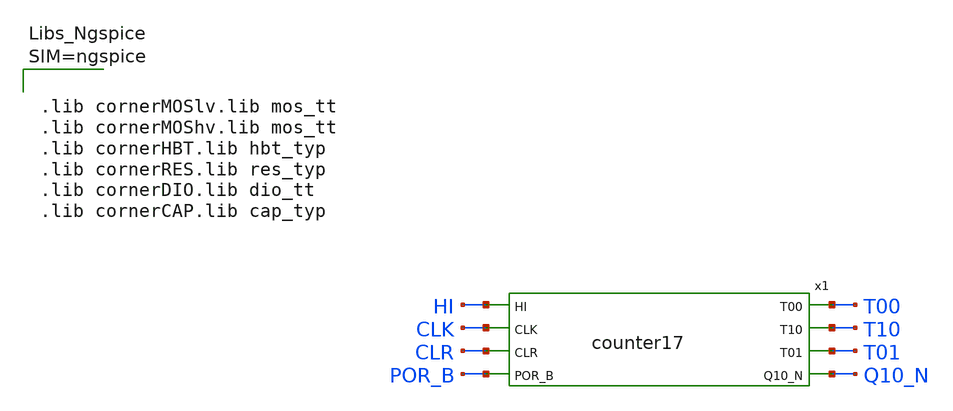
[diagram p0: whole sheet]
** sch_path: design/blocks/counter_bit/schematic/counter17_tb.sch
**.subckt counter17_tb
x1 T00 HI T10 CLK CLR T01 Q10_N POR_B VDD VSS counter17
**** begin user architecture code



.lib cornerMOSlv.lib mos_tt
.lib cornerMOShv.lib mos_tt
.lib cornerHBT.lib hbt_typ
.lib cornerRES.lib res_typ
.lib cornerDIO.lib dio_tt
.lib cornerCAP.lib cap_typ






* ============================================================
* counter17_tb -- validacion a nivel transistor de counter17 (IHP SG13G2)
* 17 x one_bit (D = (Q xor CI)&~CLR, CO = Q&CI), tomas T00 = Q13&Q11,
* T10 = Q16&Q15&Q12, T01 = Q10, Q10_N.
* Corner MOS: editar la linea .lib (mos_tt / mos_ss / ...)
* Barre T = -40/27/85 C  x  VDD = 1.08/1.2/1.32 V dentro de .control
* CLK = 50 MHz (celdas estaticas: la funcion no depende de f; con 1025 ciclos
* a 10 kHz la corrida seria de 100 ms). Flancos de subida en 10n + k*20n;
* entradas cambian en el flanco de bajada (20n + k*20n).
* Secuencia (k = numero de flanco):
*   k = 0        POR_B = 0                 -> cuenta 0 (reset asincronico)
*   k = 1..39    cuenta = k                -> se verifica Q0..Q5 en cada ciclo
*   k = 40, 41   CLR = 1                   -> cuenta 0 (borrado sincronico)
*   k = 42..51   cuenta = k - 41
*   t = 1050n    POR_B = 0 a mitad de ciclo con cuenta 10 -> Q3 y Q1 bajan sin flanco
* Las tomas (T01 = 1024, T00 = 10240, T10 = 102400 ciclos) no se alcanzan a nivel
* transistor en un tiempo razonable (>10 min por caso solo para T01): se verifican
* con el netlist exportado en Icarus (counter17_logic_tb.v). Aca se exige que
* T00, T10 y T01 no tengan glitches y que Q10_N quede en 1.
.global VDD VSS
.param vdd=1.2

* carga en las salidas: una entrada de celda (como en wd_control)
xl0 T00B T00 VDD VSS sg13g2_inv_1
xl1 T10B T10 VDD VSS sg13g2_inv_1
xl2 T01B T01 VDD VSS sg13g2_inv_1
xl3 Q10NB Q10_N VDD VSS sg13g2_inv_1

* ---------- fuentes ----------
V_VDD VDD 0 PWL(0 0 5n {vdd})
V_VSS VSS 0 0
V_HI  HI  0 {vdd}
V_CLK CLK 0 PULSE(0 {vdd} 10n 0.1n 0.1n 10n 20n)
V_POR POR_B 0 PWL(0 0 20n 0 20.01n {vdd} 1050n {vdd} 1050.01n 0)
V_CLR CLR   0 PWL(0 0 800n 0 800.01n {vdd} 840n {vdd} 840.01n 0)

.option method=gear maxord=2 reltol=1e-3
.save v(clk) v(clr) v(por_b) v(t00) v(t10) v(t01) v(q10_n) v(x1.q0) v(x1.q1) v(x1.q2) v(x1.q3) v(x1.q4) v(x1.q5)

.control
set noaskquit
compose tlist values -40 27 85
compose vlist values 1.08 1.2 1.32
let npass = 0
let ncase = 0
let it = 0
while it lt 3
 let iv = 0
 while iv lt 3
  let tt = tlist[it]
  let vv = vlist[iv]
  alterparam vdd = $&vv
  reset
  option temp = $&tt
  tran 0.1n 1100n 0 0.5n
  * reintento si ngspice aborta ('timestep too small' = artefacto numerico)
  let nt = length(time)
  let tend = time[nt-1]
  if tend lt 1090n
   echo REINTENTO T=$&tt VDD=$&vv con tmax=0.25n (aborto en t=$&tend)
   reset
   option temp = $&tt
   tran 0.05n 1100n 0 0.25n
  end
  let vh = vv/2
  * --- 1) cuenta en los bits 0..5 (muestreo a mitad de ciclo, 15 ns despues del flanco) ---
  let nok = 0
  let nchk = 0
  let k = 0
  while k lt 51
   let ts = 25n + k*20n
   if k lt 40
    let nexp = k
   else
    if k lt 42
     let nexp = 0
    else
     let nexp = k - 41
    end
   end
   meas tran b0 FIND v(x1.q0) AT=$&ts
   meas tran b1 FIND v(x1.q1) AT=$&ts
   meas tran b2 FIND v(x1.q2) AT=$&ts
   meas tran b3 FIND v(x1.q3) AT=$&ts
   meas tran b4 FIND v(x1.q4) AT=$&ts
   meas tran b5 FIND v(x1.q5) AT=$&ts
   let n = (b0 gt vh) + 2*(b1 gt vh) + 4*(b2 gt vh) + 8*(b3 gt vh) + 16*(b4 gt vh) + 32*(b5 gt vh)
   if n eq nexp
    let nok = nok + 1
   else
    echo FALLA cuenta: k=$&k leida=$&n esperada=$&nexp
   end
   let nchk = nchk + 1
   let k = k + 1
  end
  * --- 2) tomas sin glitches y Q10_N = 1 (cuenta < 1024) ---
  meas tran m00 MAX v(t00) FROM=30n TO=1040n
  meas tran m10 MAX v(t10) FROM=30n TO=1040n
  meas tran m01 MAX v(t01) FROM=30n TO=1040n
  meas tran mqn MIN v(q10_n) FROM=30n TO=1040n
  let p_tap = (m00 lt 0.3*vv) & (m10 lt 0.3*vv) & (m01 lt 0.3*vv) & (mqn gt 0.7*vv)
  * --- 3) tiempo CLK->Q del bit 0 (flanco 1, 30n) ---
  let tcq = -1
  meas tran tcq WHEN v(x1.q0)=$&vh RISE=1
  let dcq = (tcq - 30n)*1e9
  * --- 4) reset asincronico: POR_B baja en 1050n con cuenta 10 (Q3 = 1) ---
  meas tran q3a FIND v(x1.q3) AT=1045n
  let tra = -1
  meas tran tra WHEN v(x1.q3)=$&vh FALL=LAST
  let da = (tra - 1050n)*1e9
  let p_rst = (q3a gt vh) & (da gt 0) & (da lt 2)
  let pass = (nok eq nchk) & p_tap & p_rst & (dcq gt 0) & (dcq lt 2)
  if pass > 0.5
   echo CASO T=$&tt VDD=$&vv : PASS  cuenta=$&nok/$&nchk tCQ=$&dcq ns reset=$&da ns
   let npass = npass + 1
  else
   echo CASO T=$&tt VDD=$&vv : FAIL  cuenta=$&nok/$&nchk tomas=$&p_tap tCQ=$&dcq reset=$&p_rst
  end
  set wr_singlescale
  wrdata counter17_{$&tt}_{$&vv}.txt v(clk) v(clr) v(por_b) v(x1.q0) v(x1.q1) v(x1.q2) v(x1.q3)
  destroy all
  let ncase = ncase + 1
  let iv = iv + 1
 end
 let it = it + 1
end
echo ===============================================
echo RESUMEN: $&npass / $&ncase casos PASS
if npass eq ncase
 echo VEREDICTO: PASS
else
 echo VEREDICTO: FAIL
end
.endc
.end


**** end user architecture code
**.ends
.end
